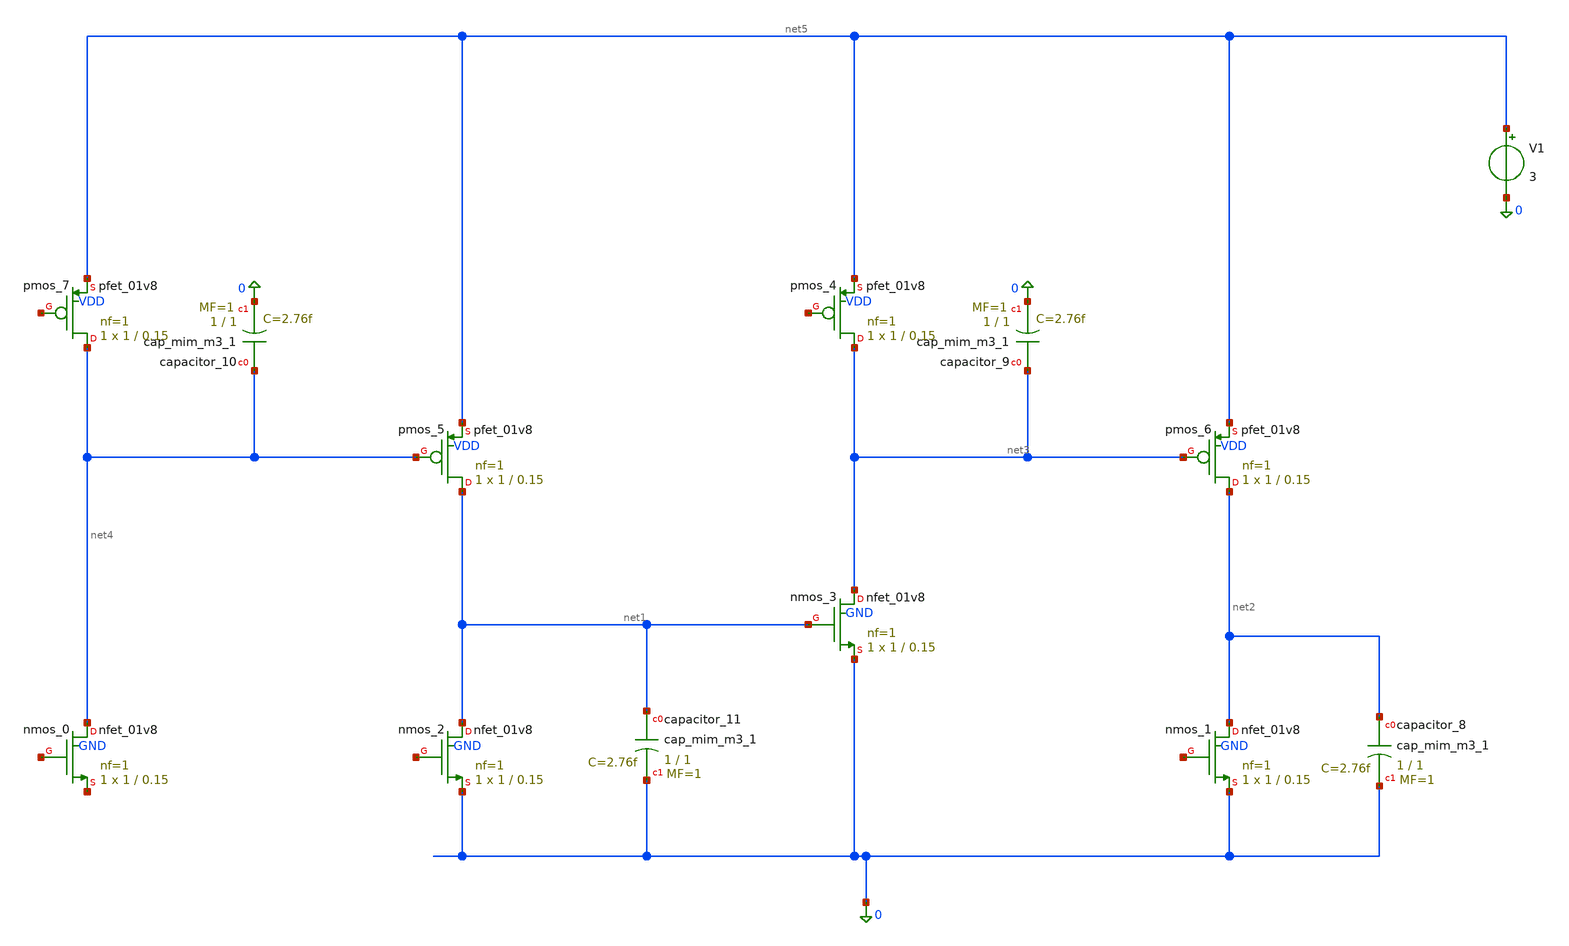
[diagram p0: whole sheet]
** sch_path: golden_netlists/10_1007_s00034-017-0630-6_05_001_crop3.sch
**.subckt 10_1007_s00034-017-0630-6_05_001_crop3
Xcapacitor_10 net4 0 sky130_fd_pr__cap_mim_m3_1 W=1 L=1 MF=1 m=1
Xcapacitor_11 net1 0 sky130_fd_pr__cap_mim_m3_1 W=1 L=1 MF=1 m=1
Xcapacitor_8 net2 0 sky130_fd_pr__cap_mim_m3_1 W=1 L=1 MF=1 m=1
Xcapacitor_9 net3 0 sky130_fd_pr__cap_mim_m3_1 W=1 L=1 MF=1 m=1
Xnmos_0 net4 net6 net7 GND sky130_fd_pr__nfet_01v8 L=0.15 W=1 nf=1 ad='int((nf+1)/2) * W/nf * 0.29' as='int((nf+2)/2) * W/nf * 0.29'
+ pd='2*int((nf+1)/2) * (W/nf + 0.29)' ps='2*int((nf+2)/2) * (W/nf + 0.29)' nrd='0.29 / W' nrs='0.29 / W'
+ sa=0 sb=0 sd=0 mult=1 m=1
Xnmos_1 net2 net8 0 GND sky130_fd_pr__nfet_01v8 L=0.15 W=1 nf=1 ad='int((nf+1)/2) * W/nf * 0.29' as='int((nf+2)/2) * W/nf * 0.29'
+ pd='2*int((nf+1)/2) * (W/nf + 0.29)' ps='2*int((nf+2)/2) * (W/nf + 0.29)' nrd='0.29 / W' nrs='0.29 / W'
+ sa=0 sb=0 sd=0 mult=1 m=1
Xnmos_2 net1 net9 0 GND sky130_fd_pr__nfet_01v8 L=0.15 W=1 nf=1 ad='int((nf+1)/2) * W/nf * 0.29' as='int((nf+2)/2) * W/nf * 0.29'
+ pd='2*int((nf+1)/2) * (W/nf + 0.29)' ps='2*int((nf+2)/2) * (W/nf + 0.29)' nrd='0.29 / W' nrs='0.29 / W'
+ sa=0 sb=0 sd=0 mult=1 m=1
Xnmos_3 net3 net1 0 GND sky130_fd_pr__nfet_01v8 L=0.15 W=1 nf=1 ad='int((nf+1)/2) * W/nf * 0.29' as='int((nf+2)/2) * W/nf * 0.29'
+ pd='2*int((nf+1)/2) * (W/nf + 0.29)' ps='2*int((nf+2)/2) * (W/nf + 0.29)' nrd='0.29 / W' nrs='0.29 / W'
+ sa=0 sb=0 sd=0 mult=1 m=1
Xpmos_4 net3 net10 net5 VDD sky130_fd_pr__pfet_01v8 L=0.15 W=1 nf=1 ad='int((1 + 1)/2) * 1 / 1 * 0.29'
+ as='int((1 + 2)/2) * 1 / 1 * 0.29' pd='2*int((1 + 1)/2) * (1 / 1 + 0.29)' ps='2*int((1 + 2)/2) * (1 / 1 + 0.29)'
+ nrd='0.29 / 1 ' nrs='0.29 / 1 ' sa=0 sb=0 sd=0 mult=1 m=1
Xpmos_5 net1 net4 net5 VDD sky130_fd_pr__pfet_01v8 L=0.15 W=1 nf=1 ad='int((1 + 1)/2) * 1 / 1 * 0.29'
+ as='int((1 + 2)/2) * 1 / 1 * 0.29' pd='2*int((1 + 1)/2) * (1 / 1 + 0.29)' ps='2*int((1 + 2)/2) * (1 / 1 + 0.29)'
+ nrd='0.29 / 1 ' nrs='0.29 / 1 ' sa=0 sb=0 sd=0 mult=1 m=1
Xpmos_6 net2 net3 net5 VDD sky130_fd_pr__pfet_01v8 L=0.15 W=1 nf=1 ad='int((1 + 1)/2) * 1 / 1 * 0.29'
+ as='int((1 + 2)/2) * 1 / 1 * 0.29' pd='2*int((1 + 1)/2) * (1 / 1 + 0.29)' ps='2*int((1 + 2)/2) * (1 / 1 + 0.29)'
+ nrd='0.29 / 1 ' nrs='0.29 / 1 ' sa=0 sb=0 sd=0 mult=1 m=1
Xpmos_7 net4 net11 net5 VDD sky130_fd_pr__pfet_01v8 L=0.15 W=1 nf=1 ad='int((1 + 1)/2) * 1 / 1 * 0.29'
+ as='int((1 + 2)/2) * 1 / 1 * 0.29' pd='2*int((1 + 1)/2) * (1 / 1 + 0.29)' ps='2*int((1 + 2)/2) * (1 / 1 + 0.29)'
+ nrd='0.29 / 1 ' nrs='0.29 / 1 ' sa=0 sb=0 sd=0 mult=1 m=1
V1 net5 0 3
**.ends
.end
